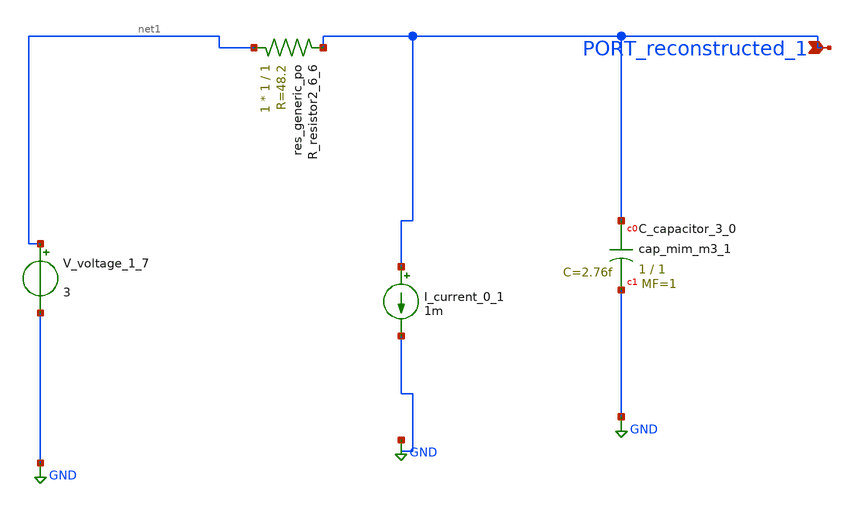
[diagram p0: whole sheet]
** sch_path: schematics/AMSNet/464.sch
**.subckt 464 PORT_reconstructed_1
*.ipin PORT_reconstructed_1
XC_capacitor_3_0 PORT_reconstructed_1 GND sky130_fd_pr__cap_mim_m3_1 W=1 L=1 MF=1 m=1
I_current_0_1 PORT_reconstructed_1 GND 1m
XR_resistor2_6_6 net1 PORT_reconstructed_1 sky130_fd_pr__res_generic_po W=1 L=1 m=1
V_voltage_1_7 net1 GND 3
**.ends
.GLOBAL GND
.end
